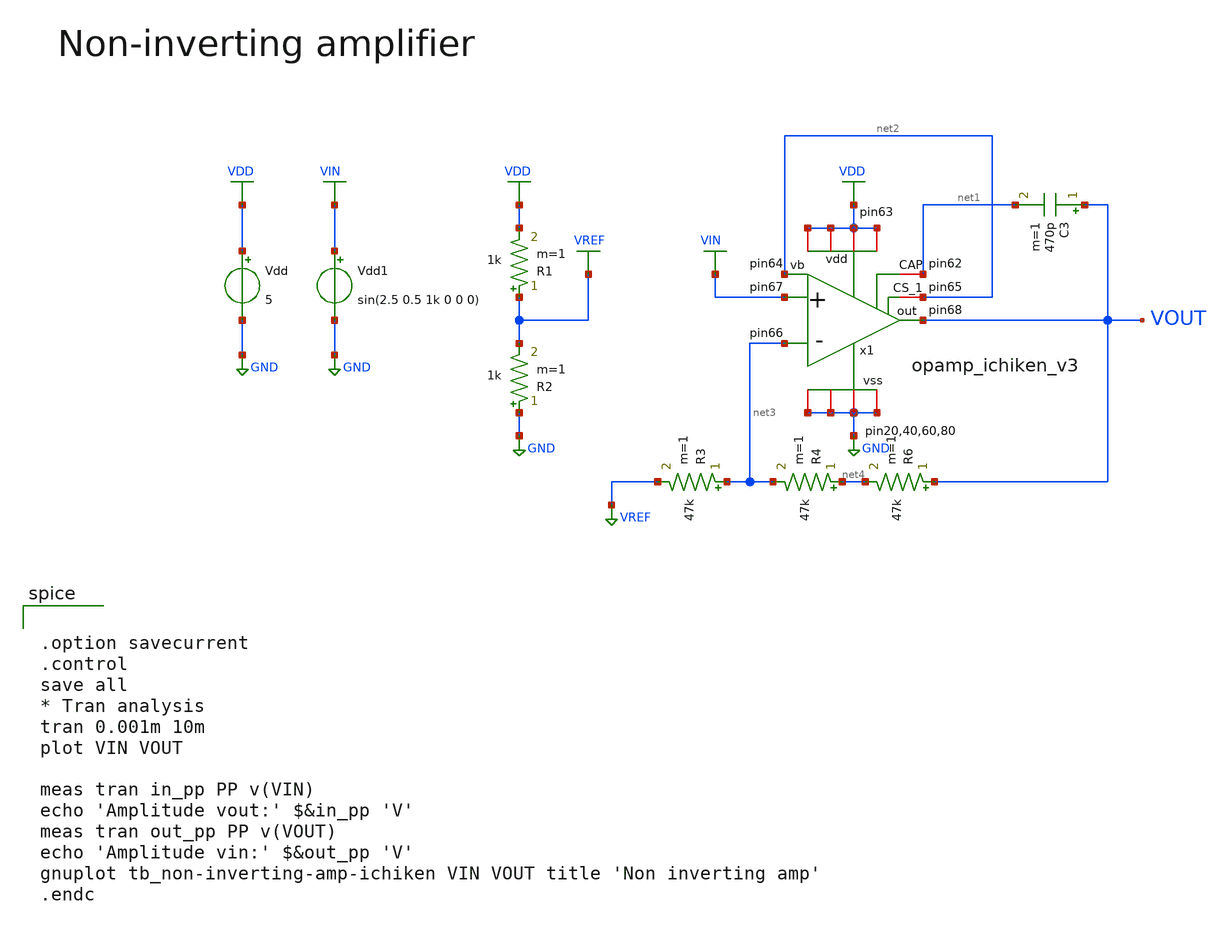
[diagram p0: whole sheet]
** sch_path: Vol.2/files/08/xschem/tb_non-inverting_amp_ichiken.sch
**.subckt tb_non-inverting_amp_ichiken
Vdd VDD GND 5
R3 net3 VREF 47k m=1
R6 VOUT net4 47k m=1
R1 VREF VDD 1k m=1
R2 GND VREF 1k m=1
Vdd1 VIN GND sin(2.5 0.5 1k 0 0 0)
x1 VDD net2 GND VIN net3 net2 VOUT net1 opamp_ichiken_v3
C3 VOUT net1 470p m=1
R4 net4 net3 47k m=1
**** begin user architecture code
 .include $::LIB/mos.lib
.include $::LIB/passive.lib
.include $::LIB/diode.lib


.option savecurrent
.control
save all
* Tran analysis
tran 0.001m 10m
plot VIN VOUT

meas tran in_pp PP v(VIN)
echo 'Amplitude vout:' $&in_pp 'V'
meas tran out_pp PP v(VOUT)
echo 'Amplitude vin:' $&out_pp 'V'
gnuplot tb_non-inverting-amp-ichiken VIN VOUT title 'Non inverting amp'
.endc


**** end user architecture code
**.ends

* expanding   symbol:  ichiken/opamp_ichiken_v3.sym # of pins=14
** sym_path: Vol.2/files/08/xschem/ichiken/opamp_ichiken_v3.sym
** sch_path: Vol.2/files/08/xschem/ichiken/opamp_ichiken_v3.sch
.subckt opamp_ichiken_v3 vdd CS_1 vss vinp vinn vb out CAP
*.iopin vdd
*.iopin vss
*.ipin vinn
*.ipin vinp
*.ipin vb
*.opin cap
*.iopin vdd
*.iopin vss
*.iopin vss
*.iopin vdd
*.iopin vss
*.iopin vdd
*.iopin vss
*.opin out
*.iopin CS_1
M4 net2 net2 vdd vdd pmos L=4u W=100u m=1
M3 net1 net2 vdd vdd pmos L=4u W=100u m=1
M2 net2 net1 net3 vss nmos L=4u W=20u m=1
M1 net1 net3 vss vss nmos L=4u W=20u m=1
M5 net4 net2 vdd vdd pmos L=4u W=100u m=1
M6 net4 net4 vss vss nmos L=4u W=20u m=1
M7 CS_1 net4 vss vss nmos L=4u W=20u m=1
M8 net1 vdd vdd vdd pmos L=4u W=24u m=1
M9 net1 vdd vdd vdd pmos L=4u W=24u m=1
M10 net1 vdd vdd vdd pmos L=4u W=24u m=1
M11 net1 vdd vdd vdd pmos L=4u W=24u m=1
M13 net2 vdd vdd vdd pmos L=4u W=24u m=1
M12 net2 vdd vdd vdd pmos L=4u W=24u m=1
M15 net2 vdd vdd vdd pmos L=4u W=24u m=1
M16 net2 vdd vdd vdd pmos L=4u W=24u m=1
M24 net4 vdd vdd vdd pmos L=4u W=24u m=1
M25 net4 vdd vdd vdd pmos L=4u W=24u m=1
M26 net4 vss vss vss nmos L=4u W=10u m=1
M27 net4 vss vss vss nmos L=4u W=10u m=1
M29 CS_1 vss vss vss nmos L=4u W=10u m=1
M30 CS_1 vss vss vss nmos L=4u W=10u m=1
M28 net7 vb vdd vdd pmos L=4u W=80u m=1
M31 net6 vinn net7 net7 pmos L=4u W=400u m=1
M32 net5 vinp net7 net7 pmos L=4u W=400u m=1
M33 net6 net6 vss vss nmos L=4u W=60u m=1
M35 net7 vdd vdd vdd pmos L=4u W=20u m=1
M36 net7 vdd vdd vdd pmos L=4u W=20u m=1
M37 net5 net7 net7 net7 pmos L=4u W=20u m=1
M38 net5 net7 net7 net7 pmos L=4u W=20u m=1
M39 net6 net7 net7 net7 pmos L=4u W=20u m=1
M40 net6 net7 net7 net7 pmos L=4u W=20u m=1
M41 net5 net7 net7 net7 pmos L=4u W=20u m=1
M42 net5 net7 net7 net7 pmos L=4u W=20u m=1
M43 net6 net7 net7 net7 pmos L=4u W=20u m=1
M44 net6 net7 net7 net7 pmos L=4u W=20u m=1
M45 net6 vss vss vss nmos L=4u W=20u m=1
M46 net6 vss vss vss nmos L=4u W=20u m=1
M47 net5 vss vss vss nmos L=4u W=20u m=1
M48 net5 vss vss vss nmos L=4u W=20u m=1
M49 vb vb vdd vdd pmos L=4u W=80u m=1
M51 net8 net8 net9 vss nmos L=4u W=25u m=1
M52 net9 net9 vss vss nmos L=4u W=25u m=1
M53 out vb vdd vdd pmos L=4u W=140u m=1
M54 out net5 vss vss nmos L=4u W=200u m=1
M55 net5 net6 vss vss nmos L=4u W=60u m=1
M56 cap net8 net5 vss nmos L=4u W=40u m=1
R1 vss net3 HR_poly W=5 L=70
M20 net2 net3 net3 vss nmos L=4u W=10u m=1
M21 net2 net3 net3 vss nmos L=4u W=10u m=1
M22 net2 net3 net3 vss nmos L=4u W=10u m=1
M23 net2 net3 net3 vss nmos L=4u W=10u m=1
M14 net1 vss vss vss nmos L=4u W=10u m=1
M17 net1 vss vss vss nmos L=4u W=10u m=1
M18 net1 vss vss vss nmos L=4u W=10u m=1
M19 net1 vss vss vss nmos L=4u W=10u m=1
M50 net8 vb vdd vdd pmos L=4u W=80u m=1
C2 out cap poly_cap W=65 L=65
.ends

.GLOBAL VDD
.GLOBAL GND
.GLOBAL VREF
.GLOBAL VIN
.end
